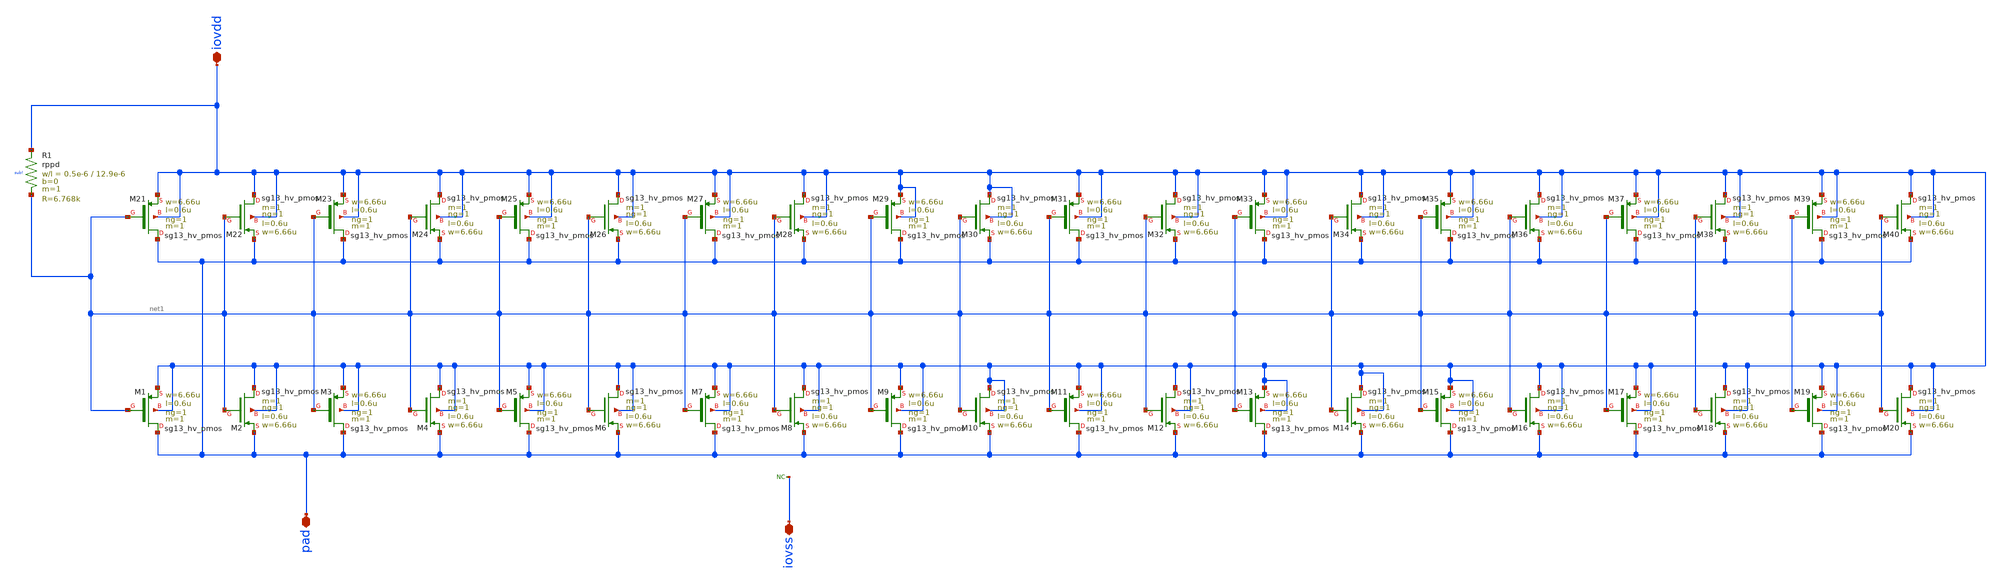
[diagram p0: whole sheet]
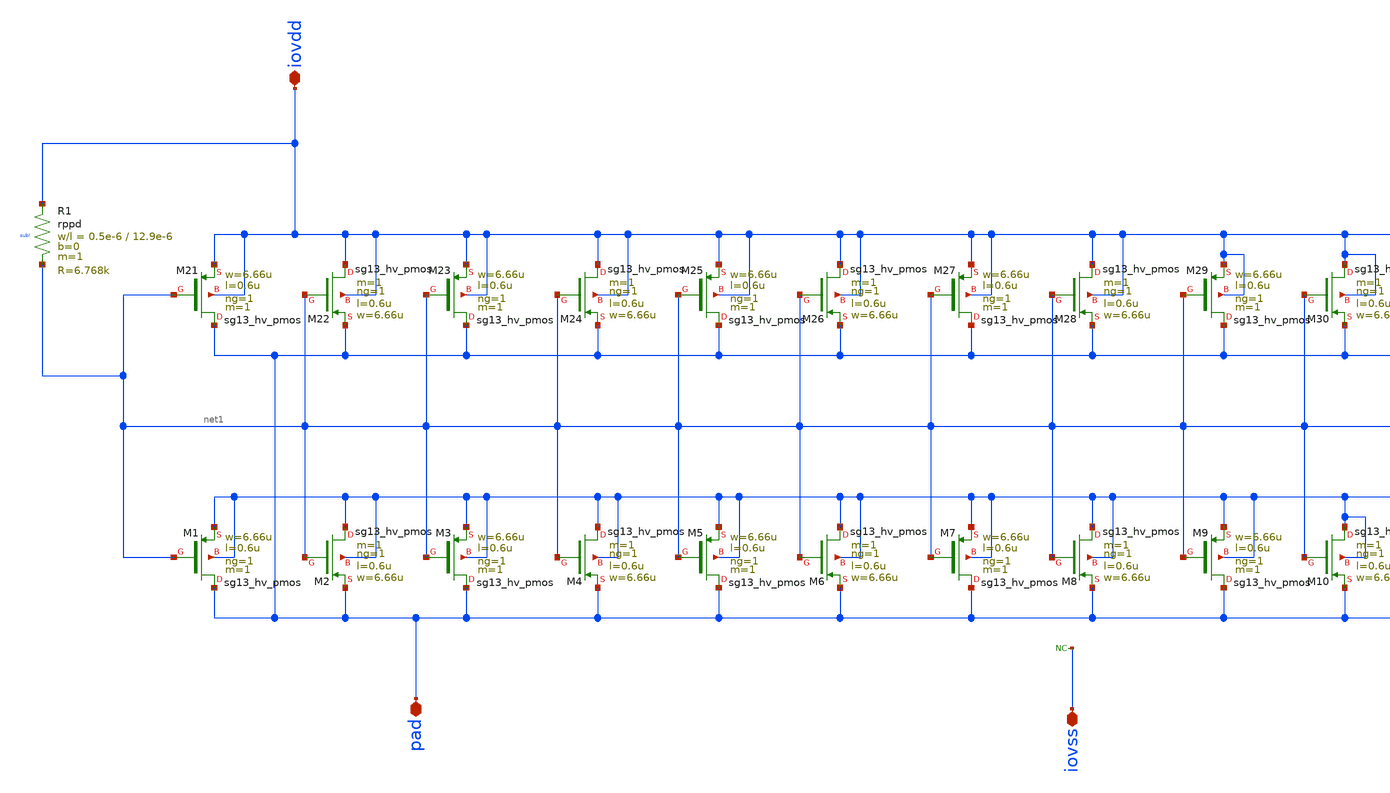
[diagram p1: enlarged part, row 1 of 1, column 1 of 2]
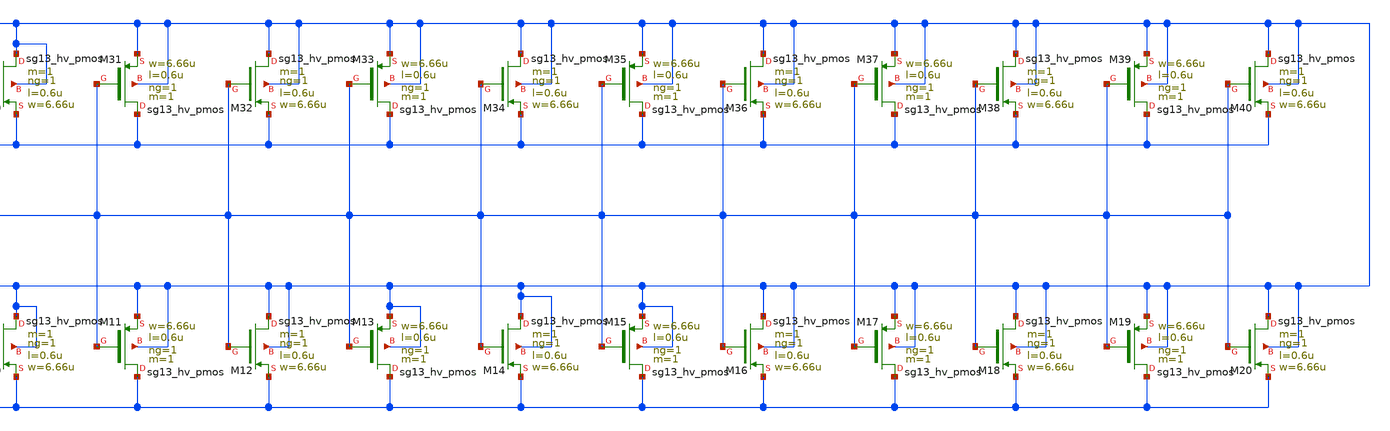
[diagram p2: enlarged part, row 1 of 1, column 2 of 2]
** sch_path: OTA_Telescopic_NO_FLATTEN/Schematics_and_Symbols/IOCells/sg13g2_Clamp_P20N0D.sch
**.subckt sg13g2_Clamp_P20N0D iovdd pad iovss
*.iopin iovdd
*.iopin pad
*.iopin iovss
XM1 pad net1 iovdd iovdd sg13_hv_pmos w=6.66u l=0.6u ng=1 m=1 mm_ok=1
XM2 iovdd net1 pad iovdd sg13_hv_pmos w=6.66u l=0.6u ng=1 m=1 mm_ok=1
XM3 pad net1 iovdd iovdd sg13_hv_pmos w=6.66u l=0.6u ng=1 m=1 mm_ok=1
XM4 iovdd net1 pad iovdd sg13_hv_pmos w=6.66u l=0.6u ng=1 m=1 mm_ok=1
XM5 pad net1 iovdd iovdd sg13_hv_pmos w=6.66u l=0.6u ng=1 m=1 mm_ok=1
XM6 iovdd net1 pad iovdd sg13_hv_pmos w=6.66u l=0.6u ng=1 m=1 mm_ok=1
XM7 pad net1 iovdd iovdd sg13_hv_pmos w=6.66u l=0.6u ng=1 m=1 mm_ok=1
XM8 iovdd net1 pad iovdd sg13_hv_pmos w=6.66u l=0.6u ng=1 m=1 mm_ok=1
XM9 pad net1 iovdd iovdd sg13_hv_pmos w=6.66u l=0.6u ng=1 m=1 mm_ok=1
XM10 iovdd net1 pad iovdd sg13_hv_pmos w=6.66u l=0.6u ng=1 m=1 mm_ok=1
XM11 pad net1 iovdd iovdd sg13_hv_pmos w=6.66u l=0.6u ng=1 m=1 mm_ok=1
XM12 iovdd net1 pad iovdd sg13_hv_pmos w=6.66u l=0.6u ng=1 m=1 mm_ok=1
XM13 pad net1 iovdd iovdd sg13_hv_pmos w=6.66u l=0.6u ng=1 m=1 mm_ok=1
XM14 iovdd net1 pad iovdd sg13_hv_pmos w=6.66u l=0.6u ng=1 m=1 mm_ok=1
XM15 pad net1 iovdd iovdd sg13_hv_pmos w=6.66u l=0.6u ng=1 m=1 mm_ok=1
XM16 iovdd net1 pad iovdd sg13_hv_pmos w=6.66u l=0.6u ng=1 m=1 mm_ok=1
XM17 pad net1 iovdd iovdd sg13_hv_pmos w=6.66u l=0.6u ng=1 m=1 mm_ok=1
XM18 iovdd net1 pad iovdd sg13_hv_pmos w=6.66u l=0.6u ng=1 m=1 mm_ok=1
XM19 pad net1 iovdd iovdd sg13_hv_pmos w=6.66u l=0.6u ng=1 m=1 mm_ok=1
XM20 iovdd net1 pad iovdd sg13_hv_pmos w=6.66u l=0.6u ng=1 m=1 mm_ok=1
XM21 pad net1 iovdd iovdd sg13_hv_pmos w=6.66u l=0.6u ng=1 m=1 mm_ok=1
XM22 iovdd net1 pad iovdd sg13_hv_pmos w=6.66u l=0.6u ng=1 m=1 mm_ok=1
XM23 pad net1 iovdd iovdd sg13_hv_pmos w=6.66u l=0.6u ng=1 m=1 mm_ok=1
XM24 iovdd net1 pad iovdd sg13_hv_pmos w=6.66u l=0.6u ng=1 m=1 mm_ok=1
XM25 pad net1 iovdd iovdd sg13_hv_pmos w=6.66u l=0.6u ng=1 m=1 mm_ok=1
XM26 iovdd net1 pad iovdd sg13_hv_pmos w=6.66u l=0.6u ng=1 m=1 mm_ok=1
XM27 pad net1 iovdd iovdd sg13_hv_pmos w=6.66u l=0.6u ng=1 m=1 mm_ok=1
XM28 iovdd net1 pad iovdd sg13_hv_pmos w=6.66u l=0.6u ng=1 m=1 mm_ok=1
XM29 pad net1 iovdd iovdd sg13_hv_pmos w=6.66u l=0.6u ng=1 m=1 mm_ok=1
XM30 iovdd net1 pad iovdd sg13_hv_pmos w=6.66u l=0.6u ng=1 m=1 mm_ok=1
XM31 pad net1 iovdd iovdd sg13_hv_pmos w=6.66u l=0.6u ng=1 m=1 mm_ok=1
XM32 iovdd net1 pad iovdd sg13_hv_pmos w=6.66u l=0.6u ng=1 m=1 mm_ok=1
XM33 pad net1 iovdd iovdd sg13_hv_pmos w=6.66u l=0.6u ng=1 m=1 mm_ok=1
XM34 iovdd net1 pad iovdd sg13_hv_pmos w=6.66u l=0.6u ng=1 m=1 mm_ok=1
XM35 pad net1 iovdd iovdd sg13_hv_pmos w=6.66u l=0.6u ng=1 m=1 mm_ok=1
XM36 iovdd net1 pad iovdd sg13_hv_pmos w=6.66u l=0.6u ng=1 m=1 mm_ok=1
XM37 pad net1 iovdd iovdd sg13_hv_pmos w=6.66u l=0.6u ng=1 m=1 mm_ok=1
XM38 iovdd net1 pad iovdd sg13_hv_pmos w=6.66u l=0.6u ng=1 m=1 mm_ok=1
XM39 pad net1 iovdd iovdd sg13_hv_pmos w=6.66u l=0.6u ng=1 m=1 mm_ok=1
XM40 iovdd net1 pad iovdd sg13_hv_pmos w=6.66u l=0.6u ng=1 m=1 mm_ok=1
XR1 iovdd net1 sub! rppd w=0.5e-6 l=12.9e-6 m=1 b=0 mm_ok=1
* noconn iovss
**.ends
.end
